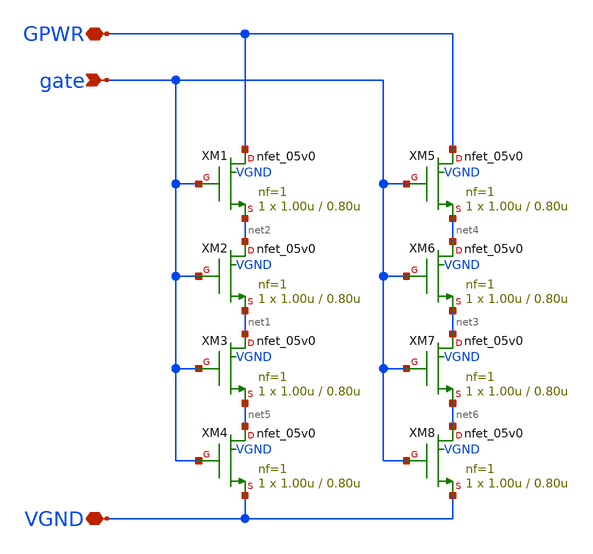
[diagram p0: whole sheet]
** sch_path: pg/gf180mcuD/tt_pg_5v0_2/xschem/discharge_5v0.sch
**.subckt discharge_5v0 GPWR VGND gate
*.iopin GPWR
*.iopin VGND
*.ipin gate
XM1 GPWR gate net2 VGND nfet_05v0 L=0.80u W=1.00u nf=1 ad='int((nf+1)/2) * W/nf * 0.18u' as='int((nf+2)/2) * W/nf * 0.18u'
+ pd='2*int((nf+1)/2) * (W/nf + 0.18u)' ps='2*int((nf+2)/2) * (W/nf + 0.18u)' nrd='0.18u / W' nrs='0.18u / W'
+ sa=0 sb=0 sd=0 m=1 par=1
XM2 net2 gate net1 VGND nfet_05v0 L=0.80u W=1.00u nf=1 ad='int((nf+1)/2) * W/nf * 0.18u' as='int((nf+2)/2) * W/nf * 0.18u'
+ pd='2*int((nf+1)/2) * (W/nf + 0.18u)' ps='2*int((nf+2)/2) * (W/nf + 0.18u)' nrd='0.18u / W' nrs='0.18u / W'
+ sa=0 sb=0 sd=0 m=1 par=1
XM3 net1 gate net5 VGND nfet_05v0 L=0.80u W=1.00u nf=1 ad='int((nf+1)/2) * W/nf * 0.18u' as='int((nf+2)/2) * W/nf * 0.18u'
+ pd='2*int((nf+1)/2) * (W/nf + 0.18u)' ps='2*int((nf+2)/2) * (W/nf + 0.18u)' nrd='0.18u / W' nrs='0.18u / W'
+ sa=0 sb=0 sd=0 m=1 par=1
XM4 net5 gate VGND VGND nfet_05v0 L=0.80u W=1.00u nf=1 ad='int((nf+1)/2) * W/nf * 0.18u' as='int((nf+2)/2) * W/nf * 0.18u'
+ pd='2*int((nf+1)/2) * (W/nf + 0.18u)' ps='2*int((nf+2)/2) * (W/nf + 0.18u)' nrd='0.18u / W' nrs='0.18u / W'
+ sa=0 sb=0 sd=0 m=1 par=1
XM5 GPWR gate net4 VGND nfet_05v0 L=0.80u W=1.00u nf=1 ad='int((nf+1)/2) * W/nf * 0.18u' as='int((nf+2)/2) * W/nf * 0.18u'
+ pd='2*int((nf+1)/2) * (W/nf + 0.18u)' ps='2*int((nf+2)/2) * (W/nf + 0.18u)' nrd='0.18u / W' nrs='0.18u / W'
+ sa=0 sb=0 sd=0 m=1 par=1
XM6 net4 gate net3 VGND nfet_05v0 L=0.80u W=1.00u nf=1 ad='int((nf+1)/2) * W/nf * 0.18u' as='int((nf+2)/2) * W/nf * 0.18u'
+ pd='2*int((nf+1)/2) * (W/nf + 0.18u)' ps='2*int((nf+2)/2) * (W/nf + 0.18u)' nrd='0.18u / W' nrs='0.18u / W'
+ sa=0 sb=0 sd=0 m=1 par=1
XM7 net3 gate net6 VGND nfet_05v0 L=0.80u W=1.00u nf=1 ad='int((nf+1)/2) * W/nf * 0.18u' as='int((nf+2)/2) * W/nf * 0.18u'
+ pd='2*int((nf+1)/2) * (W/nf + 0.18u)' ps='2*int((nf+2)/2) * (W/nf + 0.18u)' nrd='0.18u / W' nrs='0.18u / W'
+ sa=0 sb=0 sd=0 m=1 par=1
XM8 net6 gate VGND VGND nfet_05v0 L=0.80u W=1.00u nf=1 ad='int((nf+1)/2) * W/nf * 0.18u' as='int((nf+2)/2) * W/nf * 0.18u'
+ pd='2*int((nf+1)/2) * (W/nf + 0.18u)' ps='2*int((nf+2)/2) * (W/nf + 0.18u)' nrd='0.18u / W' nrs='0.18u / W'
+ sa=0 sb=0 sd=0 m=1 par=1
**.ends
.end
